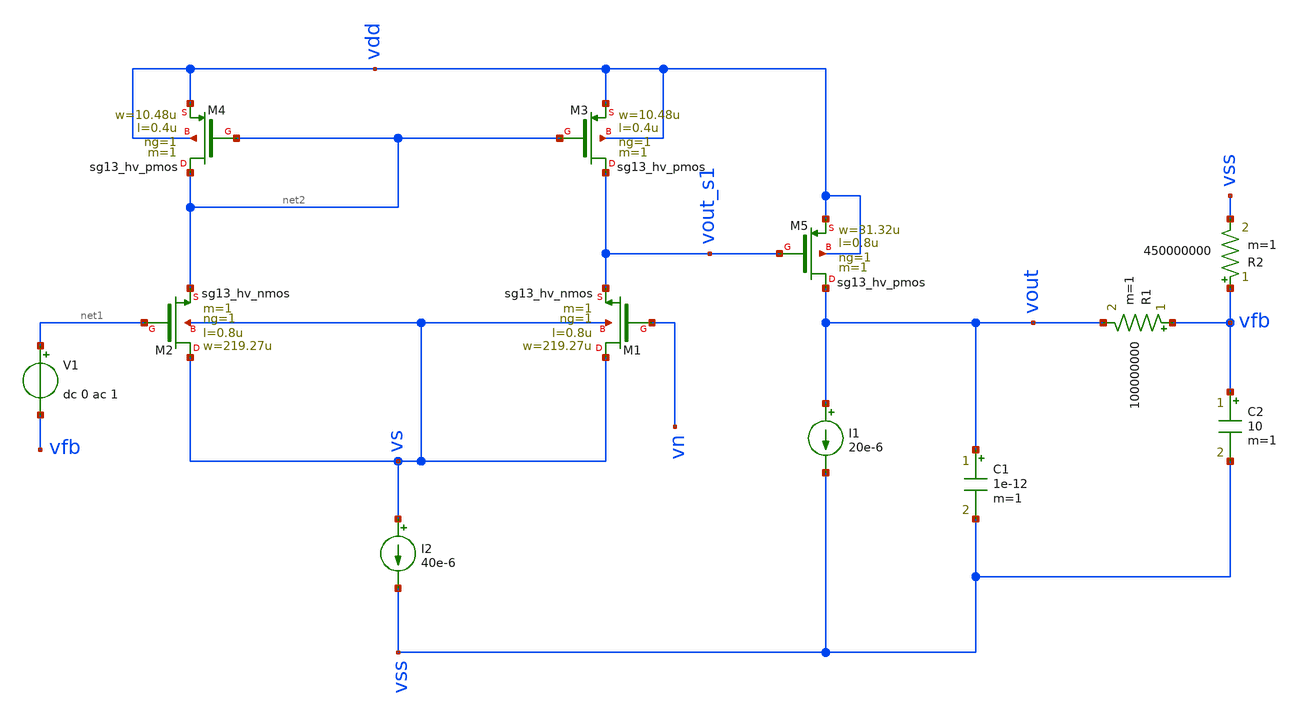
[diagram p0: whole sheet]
** sch_path: test/sstadex/xschem/stage2_OTA_tb_ihp.sch
**.subckt stage2_OTA_tb_ihp
I2 vs vss 40e-6
I1 vout vss 20e-6
C1 vout vss 1e-12 m=1
XM1 vs vn vout_s1 vs sg13_hv_nmos w=219.27u l=0.8u ng=1 m=1 mm_ok=1
XM2 vs net1 net2 vs sg13_hv_nmos w=219.27u l=0.8u ng=1 m=1 mm_ok=1
XM3 vout_s1 net2 vdd vdd sg13_hv_pmos w=10.48u l=0.4u ng=1 m=1 mm_ok=1
XM4 net2 net2 vdd vdd sg13_hv_pmos w=10.48u l=0.4u ng=1 m=1 mm_ok=1
XM5 vout vout_s1 vdd vdd sg13_hv_pmos w=31.32u l=0.8u ng=1 m=1 mm_ok=1
R1 vfb vout 100000000 m=1
C2 vfb vss 10 m=1
R2 vfb vss 450000000 m=1
V1 net1 vfb dc 0 ac 1
**** begin user architecture code



.lib /opt/pdks/ihp-sg13g2/libs.tech/ngspice/models/cornerMOShv.lib mos_tt

Vref vn 0 0.9
Vdd vdd 0 1.8
Vss vss 0 0

.param vcc=1.8

.control
ac dec 10 1 1G
plot vdb(vout)
plot phase(vout)
op
print vout vs vout_s1 vfb
.endc



**** end user architecture code
**.ends
.end
